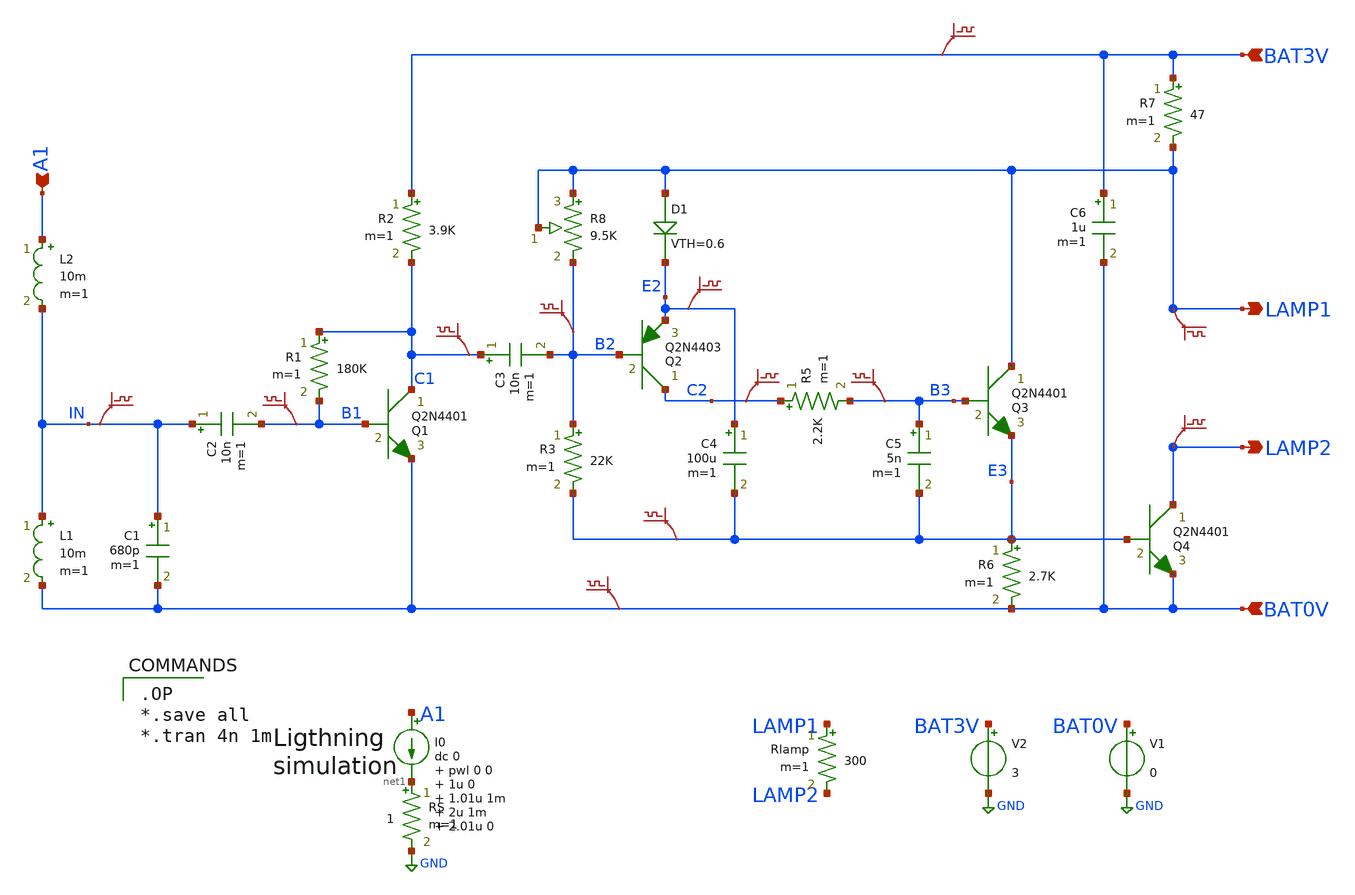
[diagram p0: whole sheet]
** sch_path: xschem_library/examples/lightning.sch
**.subckt lightning A1 BAT3V BAT0V LAMP1 LAMP2
*.ipin A1
*.ipin BAT3V
*.ipin BAT0V
*.opin LAMP1
*.opin LAMP2
L2 A1 IN 10m m=1
L1 IN BAT0V 10m m=1
C2 IN B1 10n m=1
C1 IN BAT0V 680p m=1
Q1 C1 B1 BAT0V Q2N4401 area=1 m=1
R2 BAT3V C1 3.9K m=1
R1 C1 B1 180K m=1
C3 C1 B2 10n m=1
Q2 C2 B2 E2 Q2N4403 area=1 m=1
D1 LAMP1 E2 diode VTH=0.6 RON=10 ROFF=1G
R3 B2 E3 22K m=1
C4 E2 E3 100u m=1
R5 C2 B3 2.2K m=1
C5 B3 E3 5n m=1
Q3 LAMP1 B3 E3 Q2N4401 area=1 m=1
R6 E3 BAT0V 2.7K m=1
Q4 LAMP2 E3 BAT0V Q2N4401 area=1 m=1
C6 BAT3V BAT0V 1u m=1
R7 BAT3V LAMP1 47 m=1
R8 LAMP1 B2 9.5K m=1
.save v(bat3v)
.save v(in)
.save v(b1)
.save v(e3)
.save v(b3)
.save v(b2)
.save v(bat0v)
V1 BAT0V GND 0
V2 BAT3V GND 3
.save v(c1)
.save v(c2)
.save v(lamp2)
.save v(lamp1)
Rlamp LAMP1 LAMP2 300 m=1
.save v(e2)
I0 A1 net1 dc 0 pwl 0 0 1u 0 1.01u 1m 2u 1m 2.01u 0
RS net1 GND 1 m=1
**** begin user architecture code


** you need to get the spice models for Q2N4401, Q2N4403 and D1N914
** and put them in file referenced below.
.include models_lightning.txt



.OP
*.save all
*.tran 4n 1m


**** end user architecture code
**.ends
.GLOBAL GND
.end
